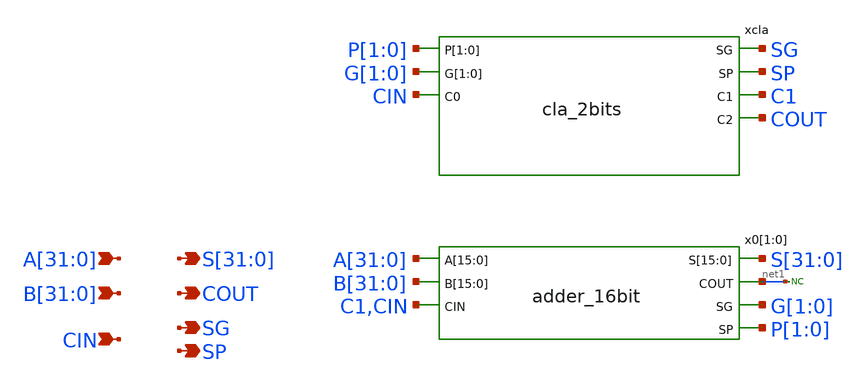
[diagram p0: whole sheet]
** sch_path: sky130A/xschem_libs/sky130_tests/adder_32bit/schematic/adder_32bit.sch
**.subckt adder_32bit
*+ A[31],A[30],A[29],A[28],A[27],A[26],A[25],A[24],A[23],A[22],A[21],A[20],A[19],A[18],A[17],A[16],A[15],A[14],A[13],A[12],A[11],A[10],A[9],A[8],A[7],A[6],A[5],A[4],A[3],A[2],A[1],A[0]
*+ B[31],B[30],B[29],B[28],B[27],B[26],B[25],B[24],B[23],B[22],B[21],B[20],B[19],B[18],B[17],B[16],B[15],B[14],B[13],B[12],B[11],B[10],B[9],B[8],B[7],B[6],B[5],B[4],B[3],B[2],B[1],B[0] CIN
*+ S[31],S[30],S[29],S[28],S[27],S[26],S[25],S[24],S[23],S[22],S[21],S[20],S[19],S[18],S[17],S[16],S[15],S[14],S[13],S[12],S[11],S[10],S[9],S[8],S[7],S[6],S[5],S[4],S[3],S[2],S[1],S[0] SP SG COUT
*.ipin
*+ A[31],A[30],A[29],A[28],A[27],A[26],A[25],A[24],A[23],A[22],A[21],A[20],A[19],A[18],A[17],A[16],A[15],A[14],A[13],A[12],A[11],A[10],A[9],A[8],A[7],A[6],A[5],A[4],A[3],A[2],A[1],A[0]
*.ipin
*+ B[31],B[30],B[29],B[28],B[27],B[26],B[25],B[24],B[23],B[22],B[21],B[20],B[19],B[18],B[17],B[16],B[15],B[14],B[13],B[12],B[11],B[10],B[9],B[8],B[7],B[6],B[5],B[4],B[3],B[2],B[1],B[0]
*.ipin CIN
*.opin
*+ S[31],S[30],S[29],S[28],S[27],S[26],S[25],S[24],S[23],S[22],S[21],S[20],S[19],S[18],S[17],S[16],S[15],S[14],S[13],S[12],S[11],S[10],S[9],S[8],S[7],S[6],S[5],S[4],S[3],S[2],S[1],S[0]
*.opin SP
*.opin SG
*.opin COUT
x0[1] A[31] A[30] A[29] A[28] A[27] A[26] A[25] A[24] A[23] A[22] A[21] A[20] A[19] A[18] A[17]
+ A[16] S[31] S[30] S[29] S[28] S[27] S[26] S[25] S[24] S[23] S[22] S[21] S[20] S[19] S[18] S[17] S[16]
+ B[31] B[30] B[29] B[28] B[27] B[26] B[25] B[24] B[23] B[22] B[21] B[20] B[19] B[18] B[17] B[16] net1 G[1]
+ C1 P[1] adder_16bit
x0[0] A[15] A[14] A[13] A[12] A[11] A[10] A[9] A[8] A[7] A[6] A[5] A[4] A[3] A[2] A[1] A[0] S[15]
+ S[14] S[13] S[12] S[11] S[10] S[9] S[8] S[7] S[6] S[5] S[4] S[3] S[2] S[1] S[0] B[15] B[14] B[13] B[12]
+ B[11] B[10] B[9] B[8] B[7] B[6] B[5] B[4] B[3] B[2] B[1] B[0] net1 G[0] CIN P[0] adder_16bit
xcla SG SP C1 P[1] P[0] COUT G[1] G[0] CIN cla_2bits
* noconn #net1
**.ends

* expanding   symbol:  sky130_tests/adder_16bit.sym # of pins=7
** sym_path: sky130_tests/adder_16bit.sym
** sch_path: sky130_tests/adder_16bit.sch
.subckt adder_16bit A[15] A[14] A[13] A[12] A[11] A[10] A[9] A[8] A[7] A[6] A[5] A[4] A[3] A[2] A[1]
+ A[0] S[15] S[14] S[13] S[12] S[11] S[10] S[9] S[8] S[7] S[6] S[5] S[4] S[3] S[2] S[1] S[0] B[15] B[14]
+ B[13] B[12] B[11] B[10] B[9] B[8] B[7] B[6] B[5] B[4] B[3] B[2] B[1] B[0] COUT SG CIN SP
*.ipin A[15],A[14],A[13],A[12],A[11],A[10],A[9],A[8],A[7],A[6],A[5],A[4],A[3],A[2],A[1],A[0]
*.ipin B[15],B[14],B[13],B[12],B[11],B[10],B[9],B[8],B[7],B[6],B[5],B[4],B[3],B[2],B[1],B[0]
*.ipin CIN
*.opin S[15],S[14],S[13],S[12],S[11],S[10],S[9],S[8],S[7],S[6],S[5],S[4],S[3],S[2],S[1],S[0]
*.opin SP
*.opin SG
*.opin COUT
xadd4[3] A[15] A[14] A[13] A[12] S[15] S[14] S[13] S[12] B[15] B[14] B[13] B[12] net1 G[3] C3 P[3]
+ adder_4bit
xadd4[2] A[11] A[10] A[9] A[8] S[11] S[10] S[9] S[8] B[11] B[10] B[9] B[8] net1 G[2] C2 P[2]
+ adder_4bit
xadd4[1] A[7] A[6] A[5] A[4] S[7] S[6] S[5] S[4] B[7] B[6] B[5] B[4] net1 G[1] C1 P[1] adder_4bit
xadd4[0] A[3] A[2] A[1] A[0] S[3] S[2] S[1] S[0] B[3] B[2] B[1] B[0] net1 G[0] CIN P[0] adder_4bit
xcla SG SP C1 P[3] P[2] P[1] P[0] C2 G[3] G[2] G[1] G[0] C3 COUT CIN cla_4bits
* noconn #net1
.ends


* expanding   symbol:  sky130_tests/cla_2bits.sym # of pins=7
** sym_path: sky130_tests/cla_2bits.sym
** sch_path: sky130_tests/cla_2bits.sch
.subckt cla_2bits SG SP C1 P[1] P[0] C2 G[1] G[0] C0
*.ipin P[1],P[0]
*.ipin G[1],G[0]
*.ipin C0
*.opin C2
*.opin C1
*.opin SG
*.opin SP
x17 G[1] VSS VSS VCC VCC net1 sky130_fd_sc_hd__inv_1
x18 P[0] C0 G[0] VSS VSS VCC VCC net3 sky130_fd_sc_hd__a21oi_1
C17 net1 0 5f m=1
C18 net3 0 5f m=1
x19 G[0] P[1] VSS VSS VCC VCC net2 sky130_fd_sc_hd__nand2_1
C19 net2 0 5f m=1
x20 P[1] P[0] C0 VSS VSS VCC VCC net4 sky130_fd_sc_hd__nand3_1
C20 net4 0 5f m=1
x21 net1 net2 VSS VSS VCC VCC SG sky130_fd_sc_hd__nand2_1
x22 P[1] P[0] VSS VSS VCC VCC SP sky130_fd_sc_hd__and2_1
x23 net3 VSS VSS VCC VCC C1 sky130_fd_sc_hd__inv_1
x24 net1 net2 net4 VSS VSS VCC VCC C2 sky130_fd_sc_hd__nand3_1
.ends


* expanding   symbol:  sky130_tests/adder_4bit.sym # of pins=7
** sym_path: sky130_tests/adder_4bit.sym
** sch_path: sky130_tests/adder_4bit.sch
.subckt adder_4bit A[3] A[2] A[1] A[0] S[3] S[2] S[1] S[0] B[3] B[2] B[1] B[0] COUT SG CIN SP
*.ipin A[3],A[2],A[1],A[0]
*.ipin B[3],B[2],B[1],B[0]
*.ipin CIN
*.opin S[3],S[2],S[1],S[0]
*.opin SP
*.opin SG
*.opin COUT
xcla SG SP C1 P[3] P[2] P[1] P[0] C2 G[3] G[2] G[1] G[0] C3 COUT CIN cla_4bits
xadd1[3] S[3] A[3] B[3] G[3] C3 P[3] adder_1bit
xadd1[2] S[2] A[2] B[2] G[2] C2 P[2] adder_1bit
xadd1[1] S[1] A[1] B[1] G[1] C1 P[1] adder_1bit
xadd1[0] S[0] A[0] B[0] G[0] CIN P[0] adder_1bit
.ends


* expanding   symbol:  sky130_tests/cla_4bits.sym # of pins=9
** sym_path: sky130_tests/cla_4bits.sym
** sch_path: sky130_tests/cla_4bits.sch
.subckt cla_4bits SG SP C1 P[3] P[2] P[1] P[0] C2 G[3] G[2] G[1] G[0] C3 C4 C0
*.ipin P[3],P[2],P[1],P[0]
*.ipin G[3],G[2],G[1],G[0]
*.ipin C0
*.opin C4
*.opin C3
*.opin C2
*.opin C1
*.opin SG
*.opin SP
x1 P[0] VSS VSS VCC VCC net4 sky130_fd_sc_hd__inv_1
x2 net5 VSS VSS VCC VCC C1 sky130_fd_sc_hd__inv_1
x3 P[1] VSS VSS VCC VCC net2 sky130_fd_sc_hd__inv_1
x4 net8 VSS VSS VCC VCC C3 sky130_fd_sc_hd__inv_1
x5 G[1] VSS VSS VCC VCC net3 sky130_fd_sc_hd__inv_1
x6 net12 VSS VSS VCC VCC net13 sky130_fd_sc_hd__inv_1
x7 G[1] P[2] G[2] VSS VSS VCC VCC net12 sky130_fd_sc_hd__a21oi_1
x8 P[3] net13 G[3] VSS VSS VCC VCC net14 sky130_fd_sc_hd__a21oi_1
x9 C0 P[0] G[0] VSS VSS VCC VCC net5 sky130_fd_sc_hd__a21oi_1
x10 P[2] C2 G[2] VSS VSS VCC VCC net8 sky130_fd_sc_hd__a21oi_1
x11 G[0] VSS VSS VCC VCC net1 sky130_fd_sc_hd__inv_1
x12 net2 net5 net3 VSS VSS VCC VCC C2 sky130_fd_sc_hd__o21ai_1
x13 net5 net10 net14 VSS VSS VCC VCC C4 sky130_fd_sc_hd__o21ai_1
x14 net1 net10 net14 VSS VSS VCC VCC SG sky130_fd_sc_hd__o21ai_1
x15 net4 net10 VSS VSS VCC VCC SP sky130_fd_sc_hd__nor2_1
x16 P[1] P[2] P[3] VSS VSS VCC VCC net10 sky130_fd_sc_hd__nand3_1
C2 net4 0 5f m=1
C1 net10 0 5f m=1
C3 net1 0 5f m=1
C4 net14 0 5f m=1
C5 net2 0 5f m=1
C6 net5 0 5f m=1
C7 net3 0 5f m=1
C8 net8 0 5f m=1
C9 net13 0 5f m=1
C10 net12 0 5f m=1
C19[3] P[3] 0 5f m=1
C19[2] P[2] 0 5f m=1
C19[1] P[1] 0 5f m=1
C19[0] P[0] 0 5f m=1
C18[3] G[3] 0 5f m=1
C18[2] G[2] 0 5f m=1
C18[1] G[1] 0 5f m=1
C18[0] G[0] 0 5f m=1
C17 C0 0 5f m=1
.ends


* expanding   symbol:  sky130_tests/adder_1bit.sym # of pins=6
** sym_path: sky130_tests/adder_1bit.sym
** sch_path: sky130_tests/adder_1bit.sch
.subckt adder_1bit S A B G CIN P
*.ipin A
*.ipin B
*.ipin CIN
*.opin S
*.opin P
*.opin G
x4 A B VSS VSS VCC VCC G sky130_fd_sc_hd__and2_1
x2 A B VSS VSS VCC VCC P sky130_fd_sc_hd__xor2_1
x3 P CIN VSS VSS VCC VCC S sky130_fd_sc_hd__xor2_1
C1 G 0 5f m=1
C2 P 0 5f m=1
C3 S 0 5f m=1
.ends

.end
